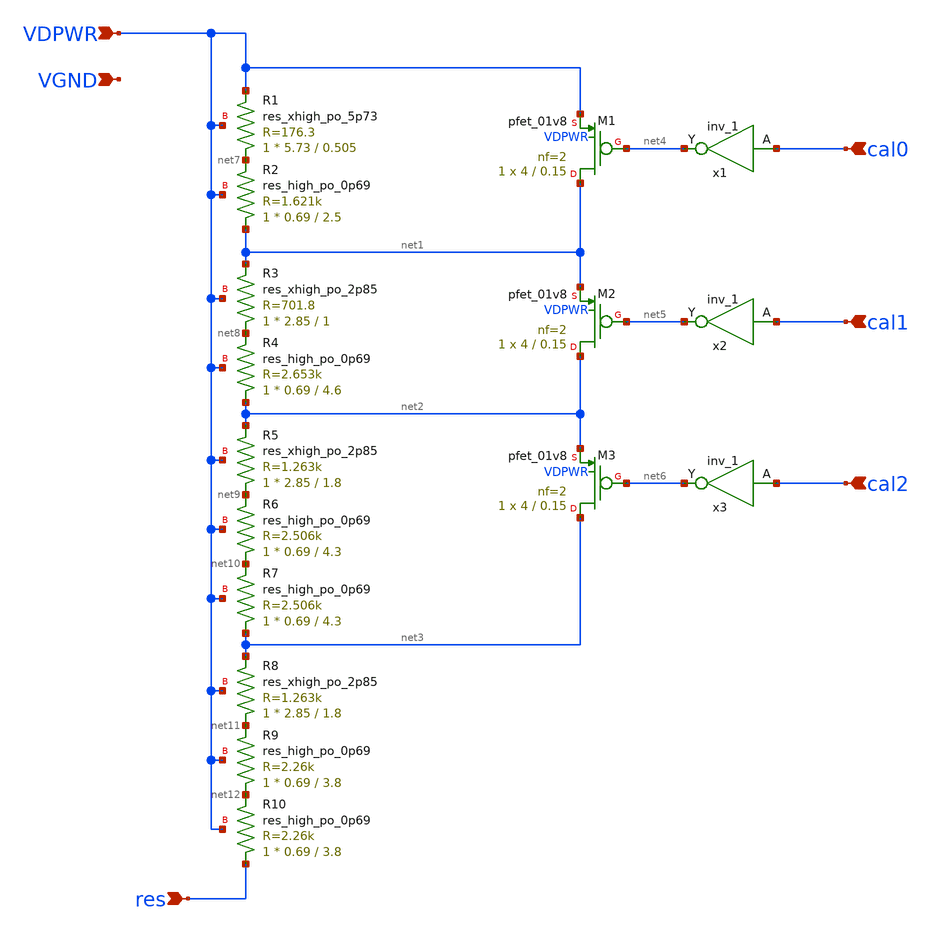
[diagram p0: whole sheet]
** sch_path: xschem/bias_resistor.sch
**.subckt bias_resistor VDPWR cal0 cal1 cal2 res VGND
*.ipin VDPWR
*.ipin cal0
*.ipin cal1
*.ipin cal2
*.ipin res
*.ipin VGND
XR2 net1 net7 VDPWR sky130_fd_pr__res_high_po_0p69 L=2.5 mult=1 m=1
XR1 net7 VDPWR VDPWR sky130_fd_pr__res_xhigh_po_5p73 L=0.505 mult=1 m=1
XR3 net8 net1 VDPWR sky130_fd_pr__res_xhigh_po_2p85 L=1 mult=1 m=1
XR4 net2 net8 VDPWR sky130_fd_pr__res_high_po_0p69 L=4.6 mult=1 m=1
XM1 net1 net4 VDPWR VDPWR sky130_fd_pr__pfet_01v8 L=0.15 W=4 nf=2 ad='int((2 + 1)/2) * 4 / 2 * 0.29'
+ as='int((2 + 2)/2) * 4 / 2 * 0.29' pd='2*int((2 + 1)/2) * (4 / 2 + 0.29)' ps='2*int((2 + 2)/2) * (4 / 2 + 0.29)'
+ nrd='0.29 / 4 ' nrs='0.29 / 4 ' sa=0 sb=0 sd=0 mult=1 m=1
XR5 net9 net2 VDPWR sky130_fd_pr__res_xhigh_po_2p85 L=1.8 mult=1 m=1
XR6 net10 net9 VDPWR sky130_fd_pr__res_high_po_0p69 L=4.3 mult=1 m=1
XR7 net3 net10 VDPWR sky130_fd_pr__res_high_po_0p69 L=4.3 mult=1 m=1
XR8 net11 net3 VDPWR sky130_fd_pr__res_xhigh_po_2p85 L=1.8 mult=1 m=1
XR9 net12 net11 VDPWR sky130_fd_pr__res_high_po_0p69 L=3.8 mult=1 m=1
XR10 res net12 VDPWR sky130_fd_pr__res_high_po_0p69 L=3.8 mult=1 m=1
XM2 net2 net5 net1 VDPWR sky130_fd_pr__pfet_01v8 L=0.15 W=4 nf=2 ad='int((2 + 1)/2) * 4 / 2 * 0.29' as='int((2 + 2)/2) * 4 / 2 * 0.29'
+ pd='2*int((2 + 1)/2) * (4 / 2 + 0.29)' ps='2*int((2 + 2)/2) * (4 / 2 + 0.29)' nrd='0.29 / 4 ' nrs='0.29 / 4 '
+ sa=0 sb=0 sd=0 mult=1 m=1
XM3 net3 net6 net2 VDPWR sky130_fd_pr__pfet_01v8 L=0.15 W=4 nf=2 ad='int((2 + 1)/2) * 4 / 2 * 0.29' as='int((2 + 2)/2) * 4 / 2 * 0.29'
+ pd='2*int((2 + 1)/2) * (4 / 2 + 0.29)' ps='2*int((2 + 2)/2) * (4 / 2 + 0.29)' nrd='0.29 / 4 ' nrs='0.29 / 4 '
+ sa=0 sb=0 sd=0 mult=1 m=1
x1 cal0 VGND VGND VDPWR VDPWR net4 sky130_fd_sc_hd__inv_1
x2 cal1 VGND VGND VDPWR VDPWR net5 sky130_fd_sc_hd__inv_1
x3 cal2 VGND VGND VDPWR VDPWR net6 sky130_fd_sc_hd__inv_1
**.ends
.end
